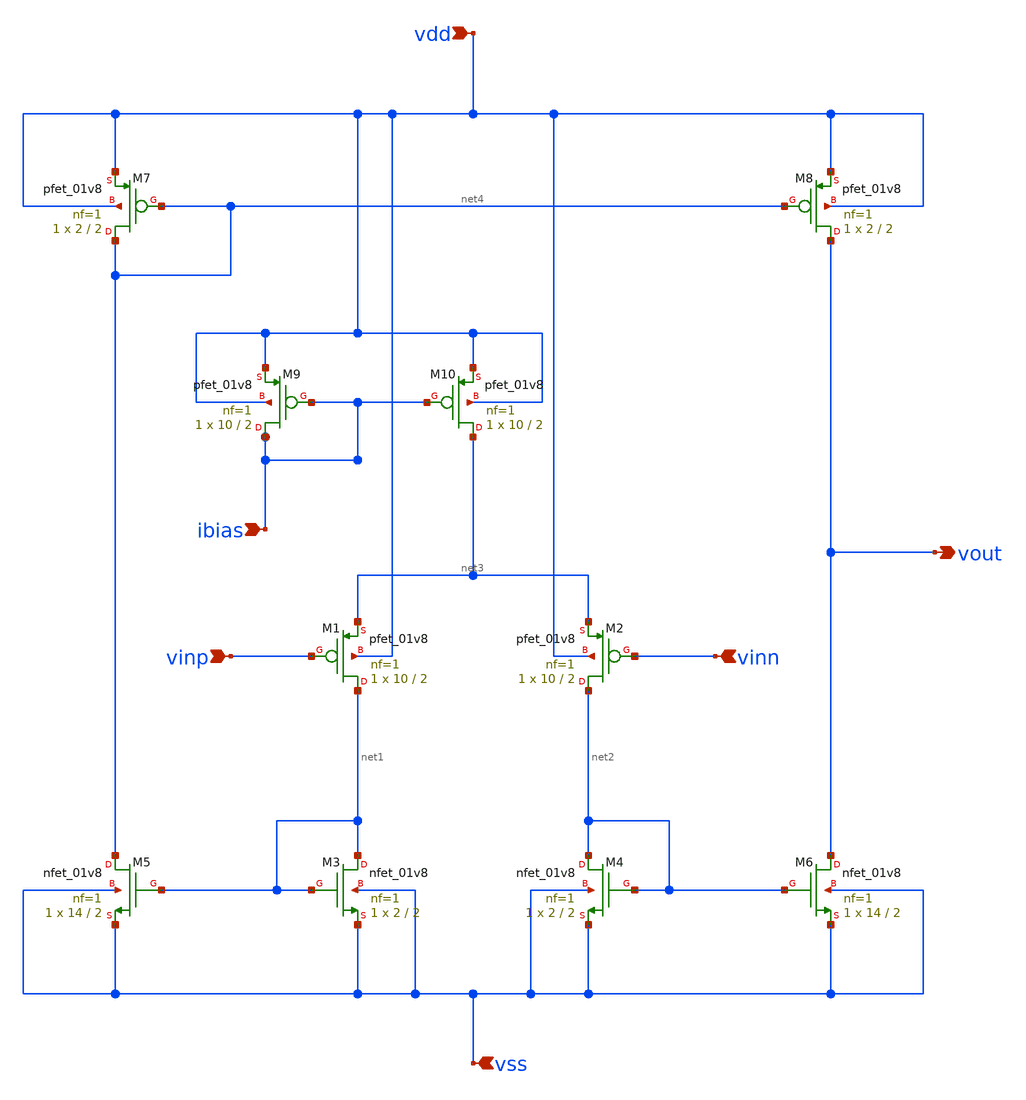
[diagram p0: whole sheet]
** sch_path: Schematic/OTA1.sch
**.subckt OTA1 vdd vinp vinn vss vout ibias
*.ipin vdd
*.ipin vinp
*.ipin vinn
*.ipin vss
*.opin vout
*.ipin ibias
XM1 net1 vinp net3 vdd sky130_fd_pr__pfet_01v8 L=2 W=10 nf=1 ad='int((1 + 1)/2) * 10 / 1 * 0.29' as='int((1 + 2)/2) * 10 / 1 * 0.29'
+ pd='2*int((1 + 1)/2) * (10 / 1 + 0.29)' ps='2*int((1 + 2)/2) * (10 / 1 + 0.29)' nrd='0.29 / 10 ' nrs='0.29 / 10 '
+ sa=0 sb=0 sd=0 mult=1 m=1
XM3 net1 net1 vss vss sky130_fd_pr__nfet_01v8 L=2 W=2 nf=1 ad='int((1 + 1)/2) * 2 / 1 * 0.29' as='int((1 + 2)/2) * 2 / 1 * 0.29'
+ pd='2*int((1 + 1)/2) * (2 / 1 + 0.29)' ps='2*int((1 + 2)/2) * (2 / 1 + 0.29)' nrd='0.29 / 2 ' nrs='0.29 / 2 '
+ sa=0 sb=0 sd=0 mult=1 m=1
XM4 net2 net2 vss vss sky130_fd_pr__nfet_01v8 L=2 W=2 nf=1 ad='int((1 + 1)/2) * 2 / 1 * 0.29' as='int((1 + 2)/2) * 2 / 1 * 0.29'
+ pd='2*int((1 + 1)/2) * (2 / 1 + 0.29)' ps='2*int((1 + 2)/2) * (2 / 1 + 0.29)' nrd='0.29 / 2 ' nrs='0.29 / 2 '
+ sa=0 sb=0 sd=0 mult=1 m=1
XM2 net2 vinn net3 vdd sky130_fd_pr__pfet_01v8 L=2 W=10 nf=1 ad='int((1 + 1)/2) * 10 / 1 * 0.29' as='int((1 + 2)/2) * 10 / 1 * 0.29'
+ pd='2*int((1 + 1)/2) * (10 / 1 + 0.29)' ps='2*int((1 + 2)/2) * (10 / 1 + 0.29)' nrd='0.29 / 10 ' nrs='0.29 / 10 '
+ sa=0 sb=0 sd=0 mult=1 m=1
XM5 net4 net1 vss vss sky130_fd_pr__nfet_01v8 L=2 W=14 nf=1 ad='int((1 + 1)/2) * 14 / 1 * 0.29' as='int((1 + 2)/2) * 14 / 1 * 0.29'
+ pd='2*int((1 + 1)/2) * (14 / 1 + 0.29)' ps='2*int((1 + 2)/2) * (14 / 1 + 0.29)' nrd='0.29 / 14 ' nrs='0.29 / 14 '
+ sa=0 sb=0 sd=0 mult=1 m=1
XM6 vout net2 vss vss sky130_fd_pr__nfet_01v8 L=2 W=14 nf=1 ad='int((1 + 1)/2) * 14 / 1 * 0.29' as='int((1 + 2)/2) * 14 / 1 * 0.29'
+ pd='2*int((1 + 1)/2) * (14 / 1 + 0.29)' ps='2*int((1 + 2)/2) * (14 / 1 + 0.29)' nrd='0.29 / 14 ' nrs='0.29 / 14 '
+ sa=0 sb=0 sd=0 mult=1 m=1
XM8 vout net4 vdd vdd sky130_fd_pr__pfet_01v8 L=2 W=2 nf=1 ad='int((1 + 1)/2) * 2 / 1 * 0.29' as='int((1 + 2)/2) * 2 / 1 * 0.29'
+ pd='2*int((1 + 1)/2) * (2 / 1 + 0.29)' ps='2*int((1 + 2)/2) * (2 / 1 + 0.29)' nrd='0.29 / 2 ' nrs='0.29 / 2 '
+ sa=0 sb=0 sd=0 mult=1 m=1
XM9 ibias ibias vdd vdd sky130_fd_pr__pfet_01v8 L=2 W=10 nf=1 ad='int((1 + 1)/2) * 10 / 1 * 0.29' as='int((1 + 2)/2) * 10 / 1 * 0.29'
+ pd='2*int((1 + 1)/2) * (10 / 1 + 0.29)' ps='2*int((1 + 2)/2) * (10 / 1 + 0.29)' nrd='0.29 / 10 ' nrs='0.29 / 10 '
+ sa=0 sb=0 sd=0 mult=1 m=1
XM7 net4 net4 vdd vdd sky130_fd_pr__pfet_01v8 L=2 W=2 nf=1 ad='int((1 + 1)/2) * 2 / 1 * 0.29' as='int((1 + 2)/2) * 2 / 1 * 0.29'
+ pd='2*int((1 + 1)/2) * (2 / 1 + 0.29)' ps='2*int((1 + 2)/2) * (2 / 1 + 0.29)' nrd='0.29 / 2 ' nrs='0.29 / 2 '
+ sa=0 sb=0 sd=0 mult=1 m=1
XM10 net3 ibias vdd vdd sky130_fd_pr__pfet_01v8 L=2 W=10 nf=1 ad='int((1 + 1)/2) * 10 / 1 * 0.29' as='int((1 + 2)/2) * 10 / 1 * 0.29'
+ pd='2*int((1 + 1)/2) * (10 / 1 + 0.29)' ps='2*int((1 + 2)/2) * (10 / 1 + 0.29)' nrd='0.29 / 10 ' nrs='0.29 / 10 '
+ sa=0 sb=0 sd=0 mult=1 m=1
**.ends
.end
